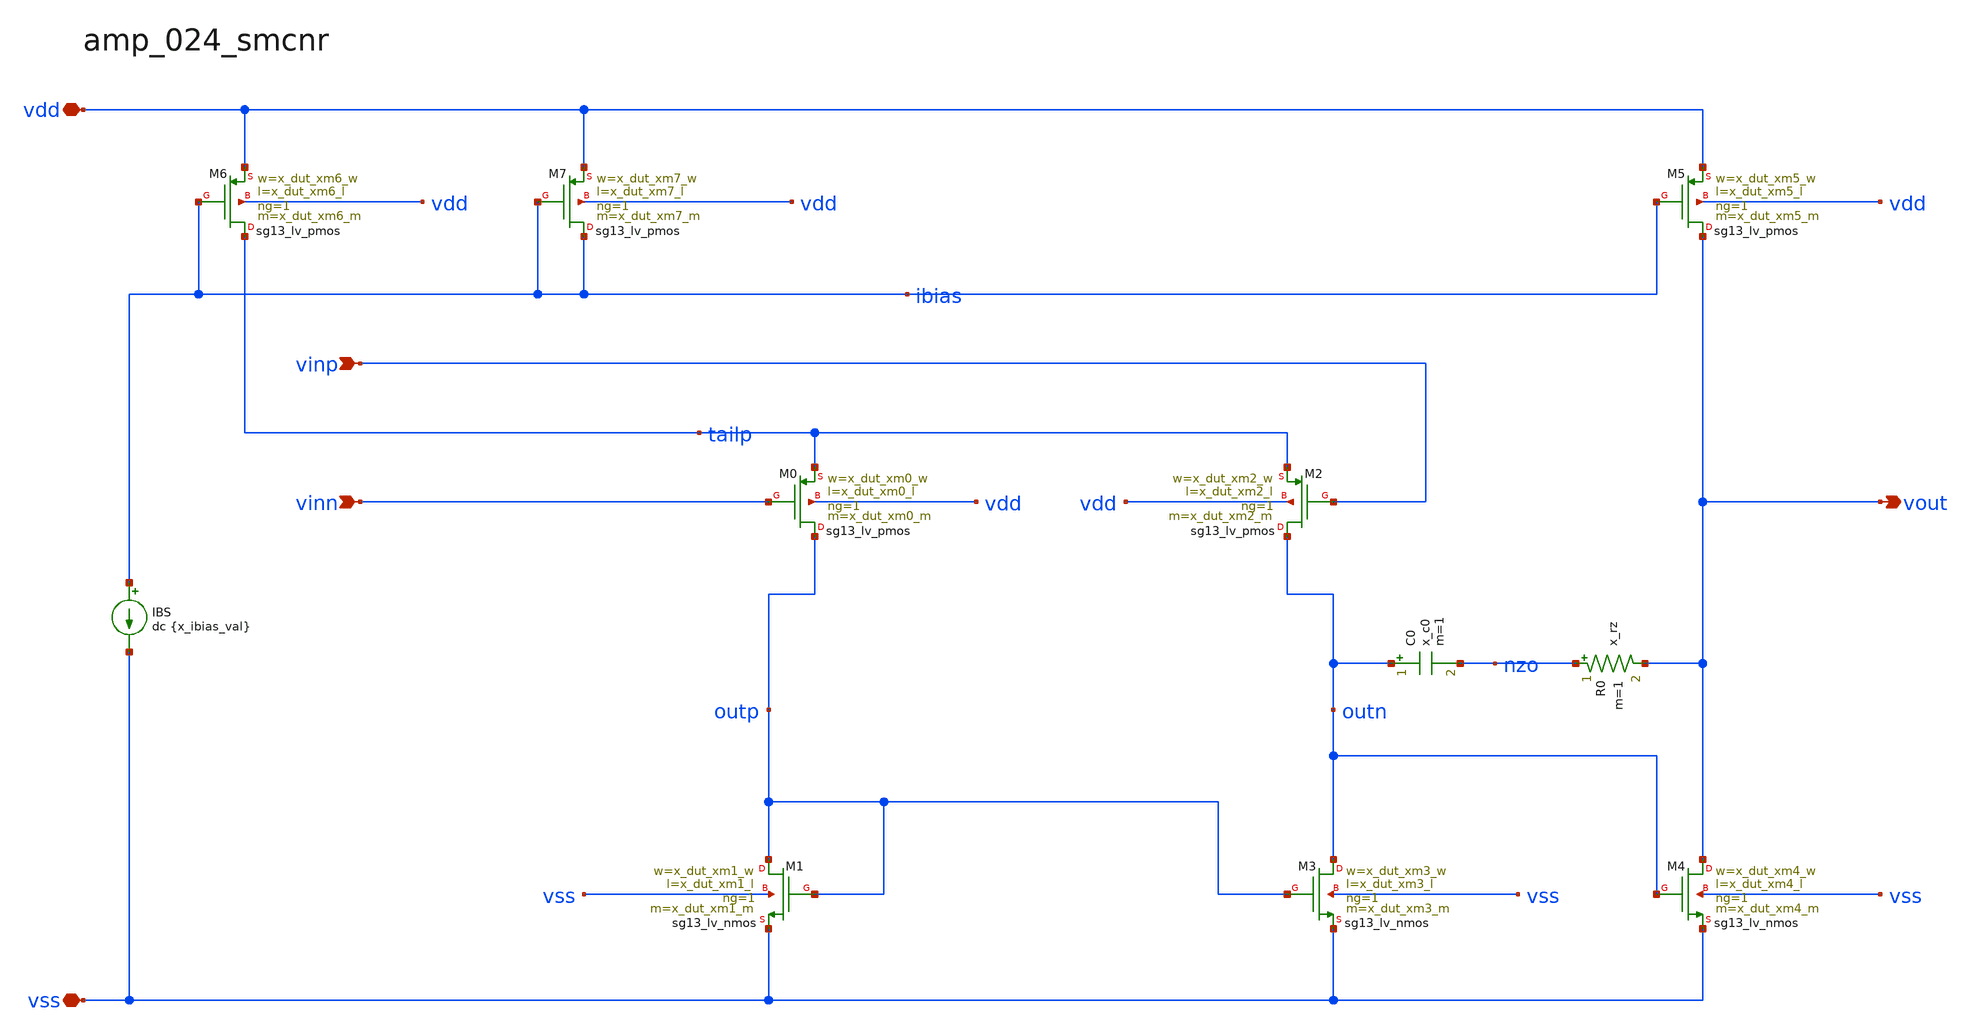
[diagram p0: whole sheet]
** sch_path: analog-db/drawings/publication/amp_024_smcnr.sch
**.subckt amp_024_smcnr vss vdd vinn vinp vout
*.iopin vss
*.iopin vdd
*.ipin vinn
*.ipin vinp
*.opin vout
XM6 tailp ibias vdd vdd sg13_lv_pmos w=x_dut_xm6_w l=x_dut_xm6_l ng=1 m=x_dut_xm6_m mm_ok=1
XM7 ibias ibias vdd vdd sg13_lv_pmos w=x_dut_xm7_w l=x_dut_xm7_l ng=1 m=x_dut_xm7_m mm_ok=1
XM5 vout ibias vdd vdd sg13_lv_pmos w=x_dut_xm5_w l=x_dut_xm5_l ng=1 m=x_dut_xm5_m mm_ok=1
XM0 outp vinn tailp vdd sg13_lv_pmos w=x_dut_xm0_w l=x_dut_xm0_l ng=1 m=x_dut_xm0_m mm_ok=1
XM2 outn vinp tailp vdd sg13_lv_pmos w=x_dut_xm2_w l=x_dut_xm2_l ng=1 m=x_dut_xm2_m mm_ok=1
XM1 outp outp vss vss sg13_lv_nmos w=x_dut_xm1_w l=x_dut_xm1_l ng=1 m=x_dut_xm1_m mm_ok=1
XM3 outn outp vss vss sg13_lv_nmos w=x_dut_xm3_w l=x_dut_xm3_l ng=1 m=x_dut_xm3_m mm_ok=1
XM4 vout outn vss vss sg13_lv_nmos w=x_dut_xm4_w l=x_dut_xm4_l ng=1 m=x_dut_xm4_m mm_ok=1
IBS ibias vss dc {x_ibias_val}
C0 outn nzo x_c0 m=1
R0 nzo vout x_rz m=1
**.ends
.end
